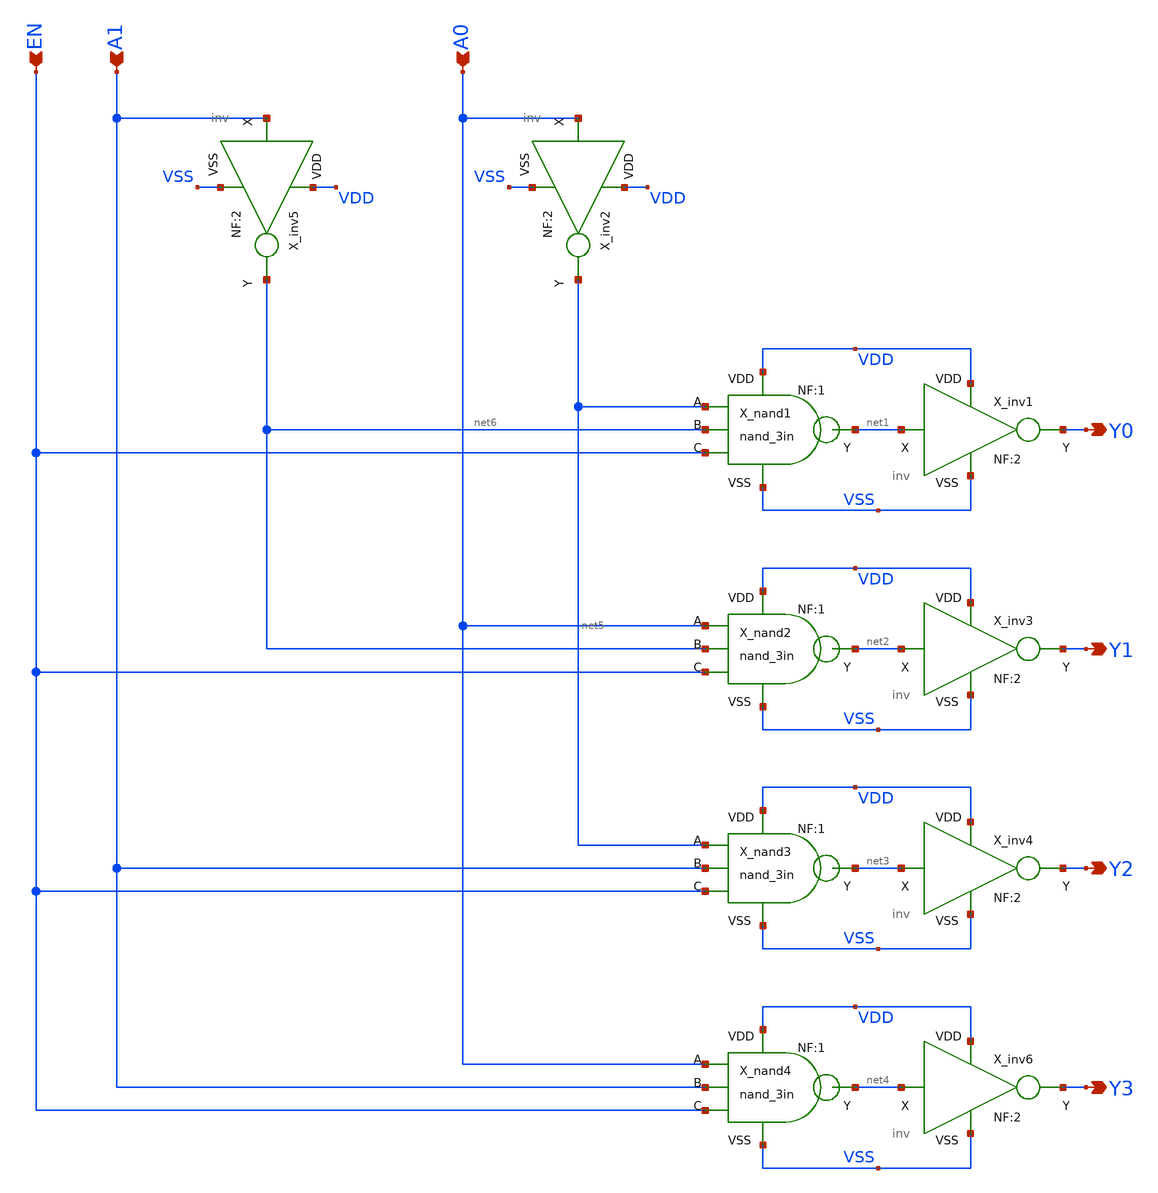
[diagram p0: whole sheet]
** sch_path: xschem_lib/DFFRAM_full_custom/dec_2to4.sch
**.subckt dec_2to4 A0 A1 EN Y0 Y1 Y2 Y3
*.ipin A0
*.ipin A1
*.ipin EN
*.opin Y0
*.opin Y1
*.opin Y2
*.opin Y3
X_inv1 net1 VDD VSS Y0 inv NF=2
X_inv3 net2 VDD VSS Y1 inv NF=2
X_inv4 net3 VDD VSS Y2 inv NF=2
X_inv6 net4 VDD VSS Y3 inv NF=2
X_inv2 A0 VDD VSS net5 inv NF=2
X_inv5 A1 VDD VSS net6 inv NF=2
X_nand1 net5 net6 EN net1 VDD VSS nand_3in NF=1
X_nand2 A0 net6 EN net2 VDD VSS nand_3in NF=1
X_nand3 net5 A1 EN net3 VDD VSS nand_3in NF=1
X_nand4 A0 A1 EN net4 VDD VSS nand_3in NF=1
**.ends

* expanding   symbol:  xschem_lib/DFFRAM_full_custom/inv.sym # of pins=4
** sym_path: xschem_lib/DFFRAM_full_custom/inv.sym
** sch_path: xschem_lib/DFFRAM_full_custom/inv.sch
.subckt inv X VDD VSS Y  NF=2
*.iopin VSS
*.ipin X
*.opin Y
*.iopin VDD
XM1 Y X VSS VSS nfet_03v3 L=0.28u W=NF*0.85u nf=NF ad='int((nf+1)/2) * W/nf * 0.18u' as='int((nf+2)/2) * W/nf * 0.18u'
+ pd='2*int((nf+1)/2) * (W/nf + 0.18u)' ps='2*int((nf+2)/2) * (W/nf + 0.18u)' nrd='0.18u / W' nrs='0.18u / W'
+ sa=0 sb=0 sd=0 m=1
XM2 Y X VDD VDD pfet_03v3 L=0.28u W=NF*1.7u nf=NF ad='int((nf+1)/2) * W/nf * 0.18u' as='int((nf+2)/2) * W/nf * 0.18u'
+ pd='2*int((nf+1)/2) * (W/nf + 0.18u)' ps='2*int((nf+2)/2) * (W/nf + 0.18u)' nrd='0.18u / W' nrs='0.18u / W'
+ sa=0 sb=0 sd=0 m=1
.ends


* expanding   symbol:  xschem_lib/DFFRAM_full_custom/nand_3in.sym # of pins=6
** sym_path: xschem_lib/DFFRAM_full_custom/nand_3in.sym
** sch_path: xschem_lib/DFFRAM_full_custom/nand_3in.sch
.subckt nand_3in A B C Y VDD VSS  NF=1
*.iopin VDD
*.opin Y
*.iopin VSS
*.ipin A
*.ipin B
*.ipin C
XM1 Y A VDD VDD pfet_03v3 L=0.28u W=NF*1.7u nf=NF ad='int((nf+1)/2) * W/nf * 0.18u' as='int((nf+2)/2) * W/nf * 0.18u'
+ pd='2*int((nf+1)/2) * (W/nf + 0.18u)' ps='2*int((nf+2)/2) * (W/nf + 0.18u)' nrd='0.18u / W' nrs='0.18u / W'
+ sa=0 sb=0 sd=0 m=1
XM4 Y A net1 VSS nfet_03v3 L=0.28u W=NF*0.85u nf=1 ad='int((nf+1)/2) * W/nf * 0.18u' as='int((nf+2)/2) * W/nf * 0.18u'
+ pd='2*int((nf+1)/2) * (W/nf + 0.18u)' ps='2*int((nf+2)/2) * (W/nf + 0.18u)' nrd='0.18u / W' nrs='0.18u / W'
+ sa=0 sb=0 sd=0 m=1
XM5 net1 B net2 VSS nfet_03v3 L=0.28u W=NF*0.85u nf=1 ad='int((nf+1)/2) * W/nf * 0.18u' as='int((nf+2)/2) * W/nf * 0.18u'
+ pd='2*int((nf+1)/2) * (W/nf + 0.18u)' ps='2*int((nf+2)/2) * (W/nf + 0.18u)' nrd='0.18u / W' nrs='0.18u / W'
+ sa=0 sb=0 sd=0 m=1
XM6 net2 C VSS VSS nfet_03v3 L=0.28u W=NF*0.85u nf=1 ad='int((nf+1)/2) * W/nf * 0.18u' as='int((nf+2)/2) * W/nf * 0.18u'
+ pd='2*int((nf+1)/2) * (W/nf + 0.18u)' ps='2*int((nf+2)/2) * (W/nf + 0.18u)' nrd='0.18u / W' nrs='0.18u / W'
+ sa=0 sb=0 sd=0 m=1
XM2 Y B VDD VDD pfet_03v3 L=0.28u W=NF*1.7u nf=NF ad='int((nf+1)/2) * W/nf * 0.18u' as='int((nf+2)/2) * W/nf * 0.18u'
+ pd='2*int((nf+1)/2) * (W/nf + 0.18u)' ps='2*int((nf+2)/2) * (W/nf + 0.18u)' nrd='0.18u / W' nrs='0.18u / W'
+ sa=0 sb=0 sd=0 m=1
XM3 Y C VDD VDD pfet_03v3 L=0.28u W=NF*1.7u nf=NF ad='int((nf+1)/2) * W/nf * 0.18u' as='int((nf+2)/2) * W/nf * 0.18u'
+ pd='2*int((nf+1)/2) * (W/nf + 0.18u)' ps='2*int((nf+2)/2) * (W/nf + 0.18u)' nrd='0.18u / W' nrs='0.18u / W'
+ sa=0 sb=0 sd=0 m=1
.ends

.end
